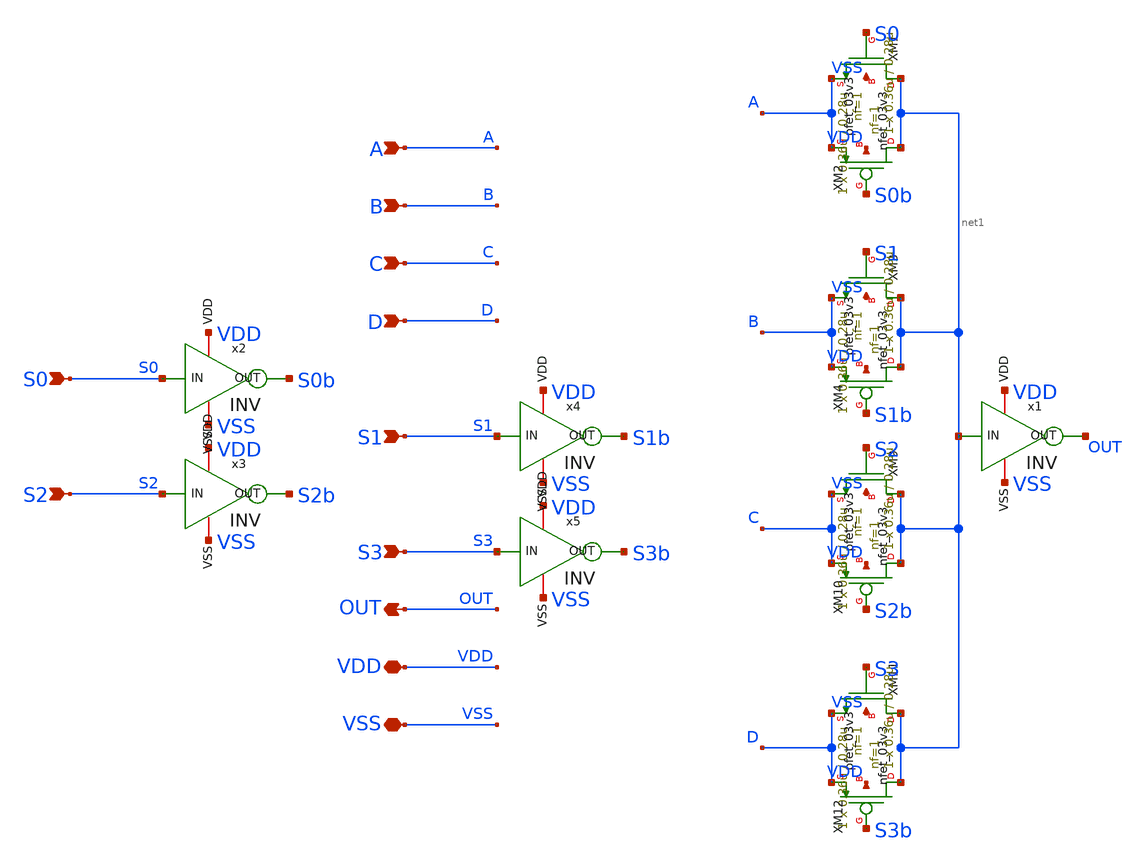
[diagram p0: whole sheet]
** sch_path: CAD4/4TG.sch
**.subckt 4TG A B S0 C D OUT S1 VDD VSS S2 S3
*.ipin A
*.ipin B
*.ipin S0
*.ipin C
*.ipin D
*.opin OUT
*.ipin S1
*.iopin VDD
*.iopin VSS
*.ipin S2
*.ipin S3
XM1 net1 S0 A VSS nfet_03v3 L=0.28u W=0.36u nf=1 ad='int((nf+1)/2) * W/nf * 0.18u' as='int((nf+2)/2) * W/nf * 0.18u'
+ pd='2*int((nf+1)/2) * (W/nf + 0.18u)' ps='2*int((nf+2)/2) * (W/nf + 0.18u)' nrd='0.18u / W' nrs='0.18u / W'
+ sa=0 sb=0 sd=0 m=1
XM2 net1 S0b A VDD pfet_03v3 L=0.28u W=0.36u nf=1 ad='int((nf+1)/2) * W/nf * 0.18u' as='int((nf+2)/2) * W/nf * 0.18u'
+ pd='2*int((nf+1)/2) * (W/nf + 0.18u)' ps='2*int((nf+2)/2) * (W/nf + 0.18u)' nrd='0.18u / W' nrs='0.18u / W'
+ sa=0 sb=0 sd=0 m=1
XM3 net1 S1 B VSS nfet_03v3 L=0.28u W=0.36u nf=1 ad='int((nf+1)/2) * W/nf * 0.18u' as='int((nf+2)/2) * W/nf * 0.18u'
+ pd='2*int((nf+1)/2) * (W/nf + 0.18u)' ps='2*int((nf+2)/2) * (W/nf + 0.18u)' nrd='0.18u / W' nrs='0.18u / W'
+ sa=0 sb=0 sd=0 m=1
XM4 net1 S1b B VDD pfet_03v3 L=0.28u W=0.36u nf=1 ad='int((nf+1)/2) * W/nf * 0.18u' as='int((nf+2)/2) * W/nf * 0.18u'
+ pd='2*int((nf+1)/2) * (W/nf + 0.18u)' ps='2*int((nf+2)/2) * (W/nf + 0.18u)' nrd='0.18u / W' nrs='0.18u / W'
+ sa=0 sb=0 sd=0 m=1
XM9 net1 S2 C VSS nfet_03v3 L=0.28u W=0.36u nf=1 ad='int((nf+1)/2) * W/nf * 0.18u' as='int((nf+2)/2) * W/nf * 0.18u'
+ pd='2*int((nf+1)/2) * (W/nf + 0.18u)' ps='2*int((nf+2)/2) * (W/nf + 0.18u)' nrd='0.18u / W' nrs='0.18u / W'
+ sa=0 sb=0 sd=0 m=1
XM10 net1 S2b C VDD pfet_03v3 L=0.28u W=0.36u nf=1 ad='int((nf+1)/2) * W/nf * 0.18u' as='int((nf+2)/2) * W/nf * 0.18u'
+ pd='2*int((nf+1)/2) * (W/nf + 0.18u)' ps='2*int((nf+2)/2) * (W/nf + 0.18u)' nrd='0.18u / W' nrs='0.18u / W'
+ sa=0 sb=0 sd=0 m=1
XM11 net1 S3 D VSS nfet_03v3 L=0.28u W=0.36u nf=1 ad='int((nf+1)/2) * W/nf * 0.18u' as='int((nf+2)/2) * W/nf * 0.18u'
+ pd='2*int((nf+1)/2) * (W/nf + 0.18u)' ps='2*int((nf+2)/2) * (W/nf + 0.18u)' nrd='0.18u / W' nrs='0.18u / W'
+ sa=0 sb=0 sd=0 m=1
XM12 net1 S3b D VDD pfet_03v3 L=0.28u W=0.36u nf=1 ad='int((nf+1)/2) * W/nf * 0.18u' as='int((nf+2)/2) * W/nf * 0.18u'
+ pd='2*int((nf+1)/2) * (W/nf + 0.18u)' ps='2*int((nf+2)/2) * (W/nf + 0.18u)' nrd='0.18u / W' nrs='0.18u / W'
+ sa=0 sb=0 sd=0 m=1
x1 VDD net1 OUT VSS INV
x2 VDD S0 S0b VSS INV
x3 VDD S2 S2b VSS INV
x4 VDD S1 S1b VSS INV
x5 VDD S3 S3b VSS INV
**.ends
.end
